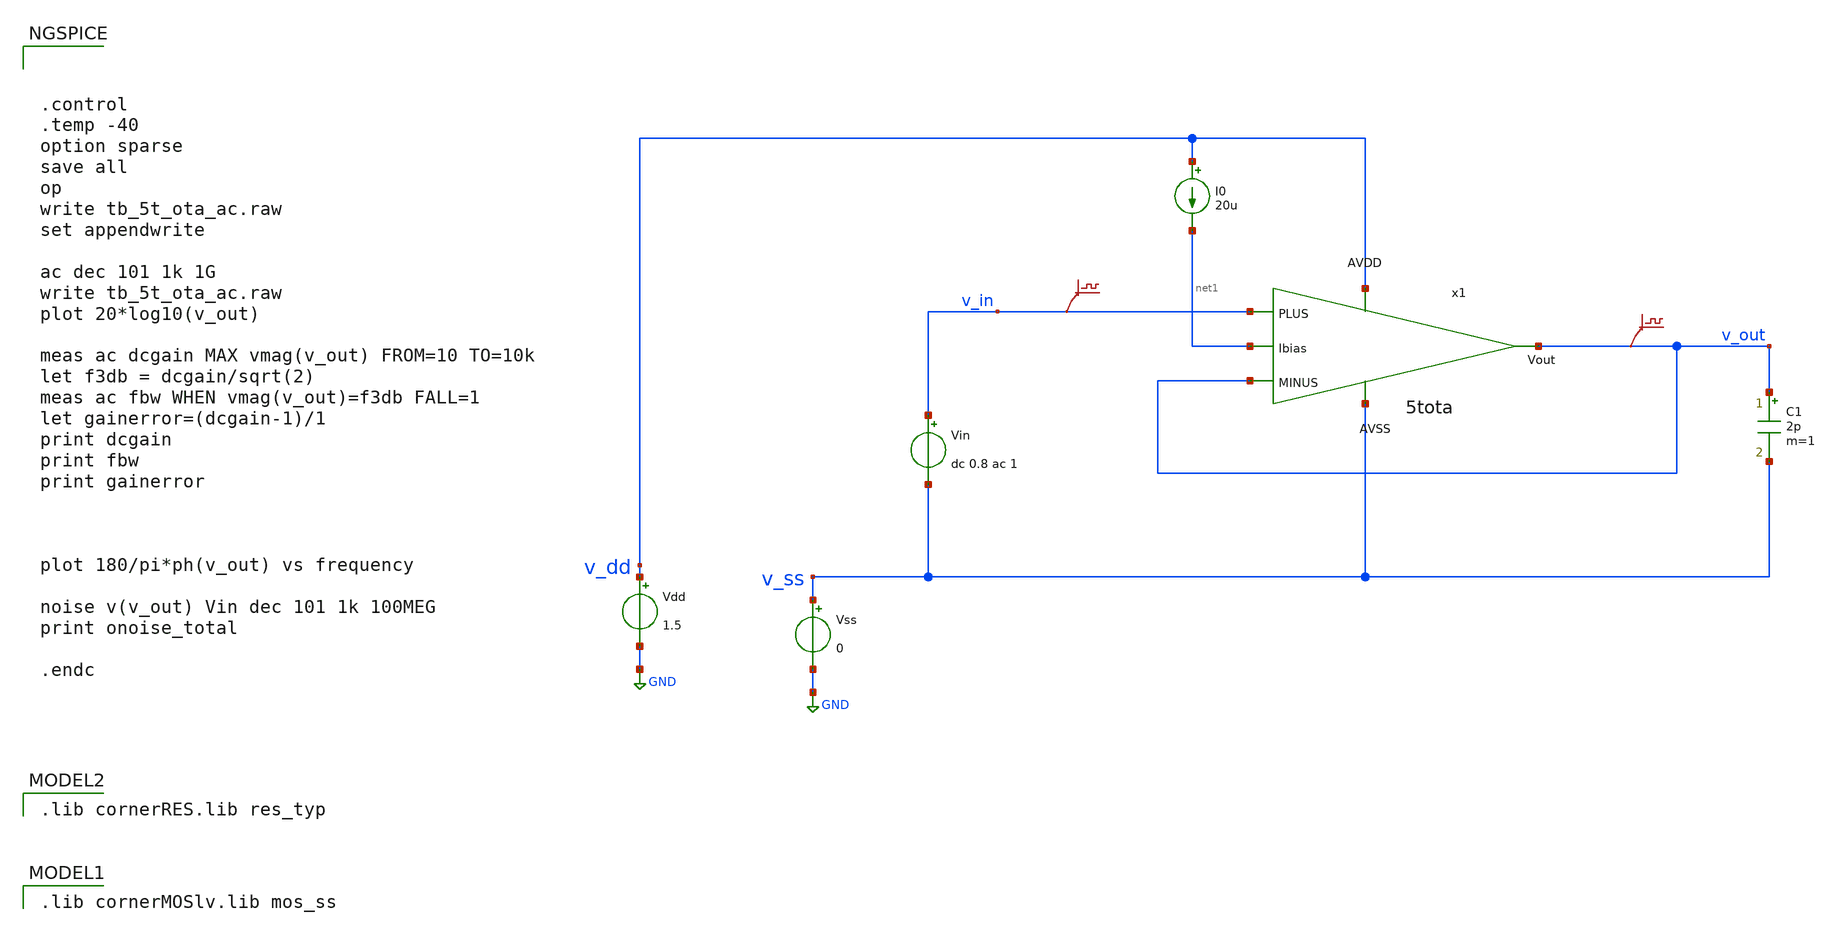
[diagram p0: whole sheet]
** sch_path: Designs/otas/1_schematics/tb_5t_ota_ac.sch
* (c) 2025 Thesis_HP, Apache-2.0 license
**.subckt tb_5t_ota_ac
Vss v_ss GND 0
Vdd v_dd GND 1.5
Vin v_in v_ss dc 0.8 ac 1
.save v(v_in)
I0 v_dd net1 20u
C1 v_out v_ss 2p m=1
.save v(v_out)
x1 v_dd v_out net1 v_in v_out v_ss 5tota
**** begin user architecture code
 .lib cornerMOSlv.lib mos_ss

 .lib cornerRES.lib res_typ




.control
.temp -40
option sparse
save all
op
write tb_5t_ota_ac.raw
set appendwrite

ac dec 101 1k 1G
write tb_5t_ota_ac.raw
plot 20*log10(v_out)

meas ac dcgain MAX vmag(v_out) FROM=10 TO=10k
let f3db = dcgain/sqrt(2)
meas ac fbw WHEN vmag(v_out)=f3db FALL=1
let gainerror=(dcgain-1)/1
print dcgain
print fbw
print gainerror



plot 180/pi*ph(v_out) vs frequency

noise v(v_out) Vin dec 101 1k 100MEG
print onoise_total

.endc


**** end user architecture code
**.ends

* expanding   symbol:  /foss/designs/thesis_hp/designs/otas/1_schematics/5tota.sym # of pins=6
** sym_path: Designs/otas/1_schematics/5tota.sym
** sch_path: Designs/otas/1_schematics/5tota.sch
.subckt 5tota AVDD Vout Ibias PLUS MINUS AVSS
*.ipin PLUS
*.ipin MINUS
*.opin Vout
*.ipin AVDD
*.ipin AVSS
*.ipin Ibias
XM1 Vout MINUS net2 AVSS sg13_lv_nmos w=2u l=5u ng=1 m=1 mm_ok=1
XM3 net1 PLUS net2 AVSS sg13_lv_nmos w=2u l=5u ng=1 m=1 mm_ok=1
XM5 Vout net1 AVDD AVDD sg13_lv_pmos w=1.5u l=5u ng=1 m=1 mm_ok=1
XM7 net1 net1 AVDD AVDD sg13_lv_pmos w=1.5u l=5u ng=1 m=1 mm_ok=1
XM6 net2 Ibias AVSS AVSS sg13_lv_nmos w=0.5u l=5u ng=1 m=1 mm_ok=1
XM2 Ibias Ibias AVSS AVSS sg13_lv_nmos w=2.5u l=5u ng=1 m=1 mm_ok=1
XM4 Vout AVSS AVSS AVSS sg13_lv_nmos w=2u l=5u ng=1 m=1 mm_ok=1
XM8 Vout AVSS AVSS AVSS sg13_lv_nmos w=2u l=5u ng=1 m=1 mm_ok=1
XM9 net1 AVSS AVSS AVSS sg13_lv_nmos w=2u l=5u ng=1 m=1 mm_ok=1
XM10 net1 AVSS AVSS AVSS sg13_lv_nmos w=2u l=5u ng=1 m=1 mm_ok=1
XM11 net2 AVSS AVSS AVSS sg13_lv_nmos w=0.5u l=5u ng=1 m=1 mm_ok=1
XM12 Vout AVDD AVDD AVDD sg13_lv_pmos w=1.5u l=5u ng=1 m=1 mm_ok=1
XM13 net1 AVDD AVDD AVDD sg13_lv_pmos w=1.5u l=5u ng=1 m=1 mm_ok=1
.ends

.GLOBAL GND
.end
